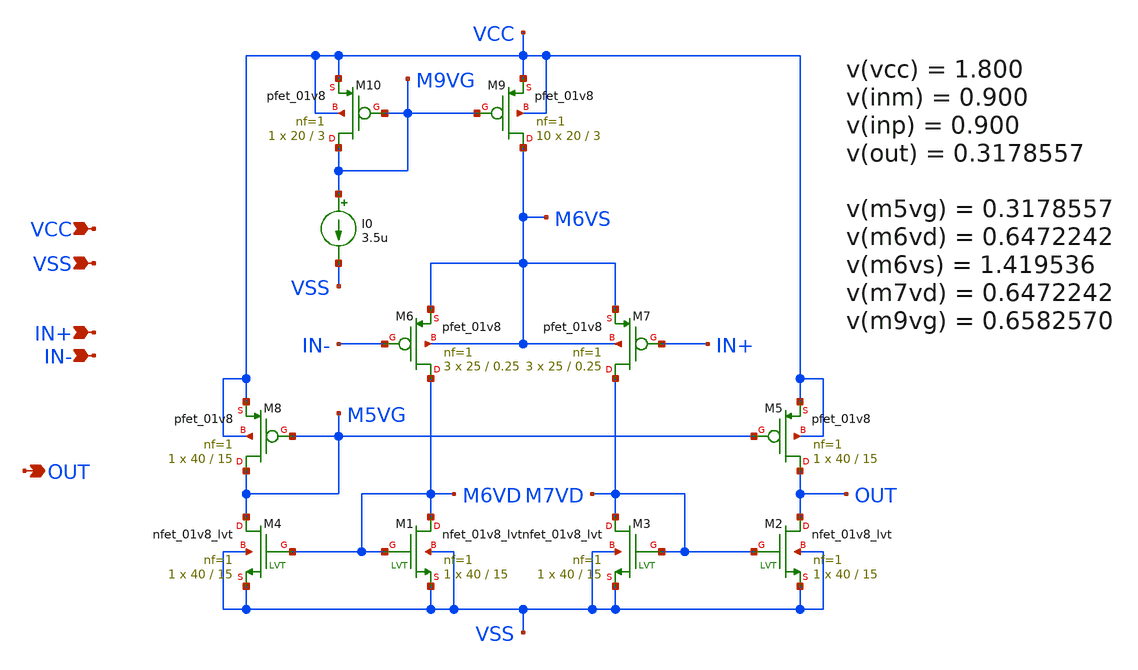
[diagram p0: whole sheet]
** sch_path: opamp_noplvt.sch
**.subckt opamp_noplvt IN+ IN- VCC VSS OUT
*.ipin IN+
*.ipin IN-
*.ipin VCC
*.ipin VSS
*.opin OUT
XM5 OUT M5VG VCC VCC sky130_fd_pr__pfet_01v8 L=15 W=40 nf=1 ad='int((nf+1)/2) * W/nf * 0.29' as='int((nf+2)/2) * W/nf * 0.29'
+ pd='2*int((nf+1)/2) * (W/nf + 0.29)' ps='2*int((nf+2)/2) * (W/nf + 0.29)' nrd='0.29 / W' nrs='0.29 / W'
+ sa=0 sb=0 sd=0 mult=1 m=1
XM8 M5VG M5VG VCC VCC sky130_fd_pr__pfet_01v8 L=15 W=40 nf=1 ad='int((nf+1)/2) * W/nf * 0.29' as='int((nf+2)/2) * W/nf * 0.29'
+ pd='2*int((nf+1)/2) * (W/nf + 0.29)' ps='2*int((nf+2)/2) * (W/nf + 0.29)' nrd='0.29 / W' nrs='0.29 / W'
+ sa=0 sb=0 sd=0 mult=1 m=1
XM9 M6VS M9VG VCC VCC sky130_fd_pr__pfet_01v8 L=3 W=20 nf=1 ad='int((nf+1)/2) * W/nf * 0.29' as='int((nf+2)/2) * W/nf * 0.29'
+ pd='2*int((nf+1)/2) * (W/nf + 0.29)' ps='2*int((nf+2)/2) * (W/nf + 0.29)' nrd='0.29 / W' nrs='0.29 / W'
+ sa=0 sb=0 sd=0 mult=10 m=10
XM10 M9VG M9VG VCC VCC sky130_fd_pr__pfet_01v8 L=3 W=20 nf=1 ad='int((nf+1)/2) * W/nf * 0.29' as='int((nf+2)/2) * W/nf * 0.29'
+ pd='2*int((nf+1)/2) * (W/nf + 0.29)' ps='2*int((nf+2)/2) * (W/nf + 0.29)' nrd='0.29 / W' nrs='0.29 / W'
+ sa=0 sb=0 sd=0 mult=1 m=1
I0 M9VG VSS 3.5u
XM1 M6VD M6VD VSS VSS sky130_fd_pr__nfet_01v8_lvt L=15 W=40 nf=1 ad='int((nf+1)/2) * W/nf * 0.29' as='int((nf+2)/2) * W/nf * 0.29'
+ pd='2*int((nf+1)/2) * (W/nf + 0.29)' ps='2*int((nf+2)/2) * (W/nf + 0.29)' nrd='0.29 / W' nrs='0.29 / W'
+ sa=0 sb=0 sd=0 mult=1 m=1
XM2 OUT M7VD VSS VSS sky130_fd_pr__nfet_01v8_lvt L=15 W=40 nf=1 ad='int((nf+1)/2) * W/nf * 0.29' as='int((nf+2)/2) * W/nf * 0.29'
+ pd='2*int((nf+1)/2) * (W/nf + 0.29)' ps='2*int((nf+2)/2) * (W/nf + 0.29)' nrd='0.29 / W' nrs='0.29 / W'
+ sa=0 sb=0 sd=0 mult=1 m=1
XM3 M7VD M7VD VSS VSS sky130_fd_pr__nfet_01v8_lvt L=15 W=40 nf=1 ad='int((nf+1)/2) * W/nf * 0.29' as='int((nf+2)/2) * W/nf * 0.29'
+ pd='2*int((nf+1)/2) * (W/nf + 0.29)' ps='2*int((nf+2)/2) * (W/nf + 0.29)' nrd='0.29 / W' nrs='0.29 / W'
+ sa=0 sb=0 sd=0 mult=1 m=1
XM4 M5VG M6VD VSS VSS sky130_fd_pr__nfet_01v8_lvt L=15 W=40 nf=1 ad='int((nf+1)/2) * W/nf * 0.29' as='int((nf+2)/2) * W/nf * 0.29'
+ pd='2*int((nf+1)/2) * (W/nf + 0.29)' ps='2*int((nf+2)/2) * (W/nf + 0.29)' nrd='0.29 / W' nrs='0.29 / W'
+ sa=0 sb=0 sd=0 mult=1 m=1
XM6 M6VD IN- M6VS M6VS sky130_fd_pr__pfet_01v8 L=0.25 W=25 nf=1 ad='int((nf+1)/2) * W/nf * 0.29' as='int((nf+2)/2) * W/nf * 0.29'
+ pd='2*int((nf+1)/2) * (W/nf + 0.29)' ps='2*int((nf+2)/2) * (W/nf + 0.29)' nrd='0.29 / W' nrs='0.29 / W'
+ sa=0 sb=0 sd=0 mult=3 m=3
XM7 M7VD IN+ M6VS M6VS sky130_fd_pr__pfet_01v8 L=0.25 W=25 nf=1 ad='int((nf+1)/2) * W/nf * 0.29' as='int((nf+2)/2) * W/nf * 0.29'
+ pd='2*int((nf+1)/2) * (W/nf + 0.29)' ps='2*int((nf+2)/2) * (W/nf + 0.29)' nrd='0.29 / W' nrs='0.29 / W'
+ sa=0 sb=0 sd=0 mult=3 m=3
**.ends
.end
